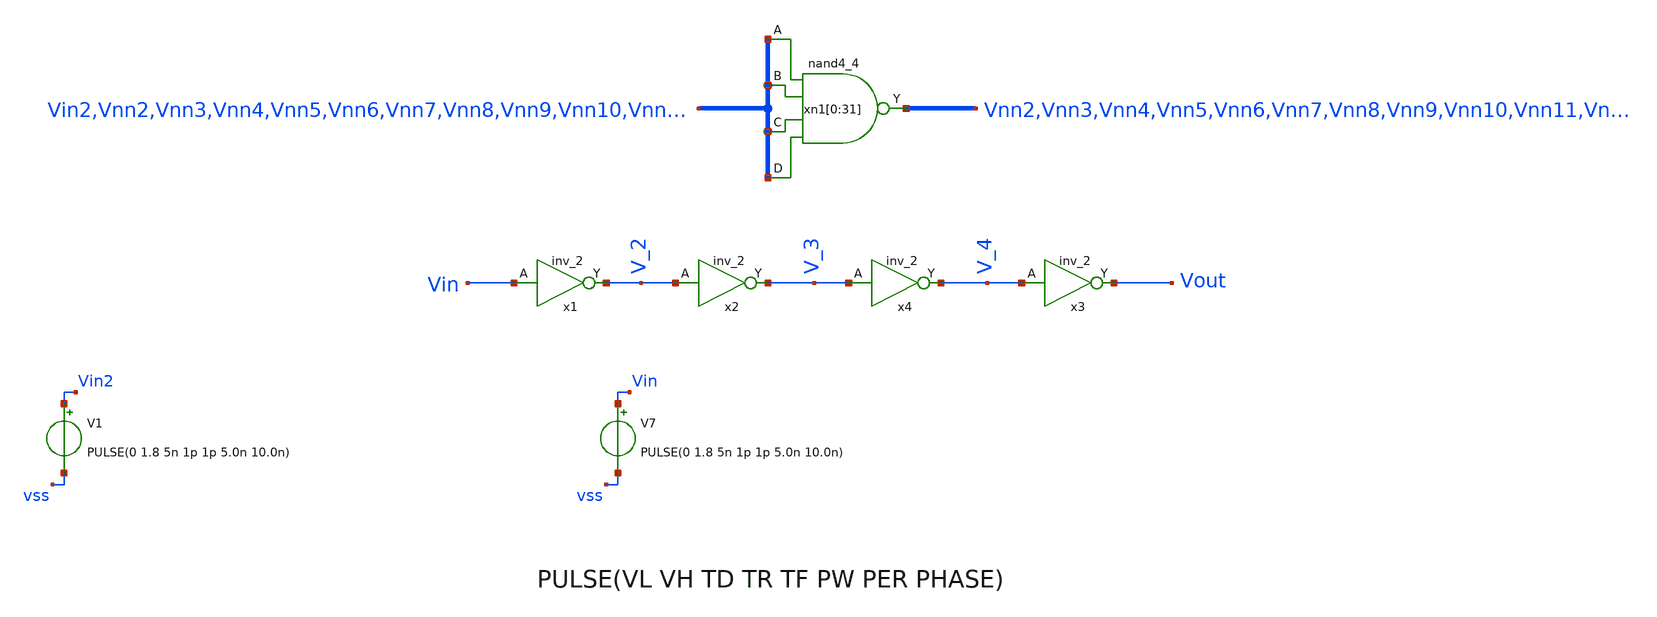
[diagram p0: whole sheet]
** sch_path: TDC_test.sch
.lib $::SKYWATER_MODELS/sky130.lib.spice tt
.include $::SKYWATER_STDCELLS/sky130_fd_sc_hd.spice

**.subckt TDC_test
x1 Vin VSS VSS VCC VCC V_2 sky130_fd_sc_hd__inv_2
x2 V_2 VSS VSS VCC VCC V_3 sky130_fd_sc_hd__inv_2
x3 V_4 VSS VSS VCC VCC Vout sky130_fd_sc_hd__inv_2
V7 Vin vss PULSE(0 1.8 5n 1p 1p 5.0n 10.0n)
x4 V_3 VSS VSS VCC VCC V_4 sky130_fd_sc_hd__inv_2
V1 Vin2 vss PULSE(0 1.8 5n 1p 1p 5.0n 10.0n)
xn1[0] Vin2 Vin2 Vin2 Vin2 VSS VSS VCC VCC Vnn2 sky130_fd_sc_hd__nand4_4
xn1[1] Vnn2 Vnn2 Vnn2 Vnn2 VSS VSS VCC VCC Vnn3 sky130_fd_sc_hd__nand4_4
xn1[2] Vnn3 Vnn3 Vnn3 Vnn3 VSS VSS VCC VCC Vnn4 sky130_fd_sc_hd__nand4_4
xn1[3] Vnn4 Vnn4 Vnn4 Vnn4 VSS VSS VCC VCC Vnn5 sky130_fd_sc_hd__nand4_4
xn1[4] Vnn5 Vnn5 Vnn5 Vnn5 VSS VSS VCC VCC Vnn6 sky130_fd_sc_hd__nand4_4
xn1[5] Vnn6 Vnn6 Vnn6 Vnn6 VSS VSS VCC VCC Vnn7 sky130_fd_sc_hd__nand4_4
xn1[6] Vnn7 Vnn7 Vnn7 Vnn7 VSS VSS VCC VCC Vnn8 sky130_fd_sc_hd__nand4_4
xn1[7] Vnn8 Vnn8 Vnn8 Vnn8 VSS VSS VCC VCC Vnn9 sky130_fd_sc_hd__nand4_4
xn1[8] Vnn9 Vnn9 Vnn9 Vnn9 VSS VSS VCC VCC Vnn10 sky130_fd_sc_hd__nand4_4
xn1[9] Vnn10 Vnn10 Vnn10 Vnn10 VSS VSS VCC VCC Vnn11 sky130_fd_sc_hd__nand4_4
xn1[10] Vnn11 Vnn11 Vnn11 Vnn11 VSS VSS VCC VCC Vnn12 sky130_fd_sc_hd__nand4_4
xn1[11] Vnn12 Vnn12 Vnn12 Vnn12 VSS VSS VCC VCC Vnn13 sky130_fd_sc_hd__nand4_4
xn1[12] Vnn13 Vnn13 Vnn13 Vnn13 VSS VSS VCC VCC Vnn14 sky130_fd_sc_hd__nand4_4
xn1[13] Vnn14 Vnn14 Vnn14 Vnn14 VSS VSS VCC VCC Vnn15 sky130_fd_sc_hd__nand4_4
xn1[14] Vnn15 Vnn15 Vnn15 Vnn15 VSS VSS VCC VCC Vnn16 sky130_fd_sc_hd__nand4_4
xn1[15] Vnn16 Vnn16 Vnn16 Vnn16 VSS VSS VCC VCC Vnn17 sky130_fd_sc_hd__nand4_4
xn1[16] Vnn17 Vnn17 Vnn17 Vnn17 VSS VSS VCC VCC Vnn18 sky130_fd_sc_hd__nand4_4
xn1[17] Vnn18 Vnn18 Vnn18 Vnn18 VSS VSS VCC VCC Vnn19 sky130_fd_sc_hd__nand4_4
xn1[18] Vnn19 Vnn19 Vnn19 Vnn19 VSS VSS VCC VCC Vnn20 sky130_fd_sc_hd__nand4_4
xn1[19] Vnn20 Vnn20 Vnn20 Vnn20 VSS VSS VCC VCC Vnn21 sky130_fd_sc_hd__nand4_4
xn1[20] Vnn21 Vnn21 Vnn21 Vnn21 VSS VSS VCC VCC Vnn22 sky130_fd_sc_hd__nand4_4
xn1[21] Vnn22 Vnn22 Vnn22 Vnn22 VSS VSS VCC VCC Vnn23 sky130_fd_sc_hd__nand4_4
xn1[22] Vnn23 Vnn23 Vnn23 Vnn23 VSS VSS VCC VCC Vnn24 sky130_fd_sc_hd__nand4_4
xn1[23] Vnn24 Vnn24 Vnn24 Vnn24 VSS VSS VCC VCC Vnn25 sky130_fd_sc_hd__nand4_4
xn1[24] Vnn25 Vnn25 Vnn25 Vnn25 VSS VSS VCC VCC Vnn26 sky130_fd_sc_hd__nand4_4
xn1[25] Vnn26 Vnn26 Vnn26 Vnn26 VSS VSS VCC VCC Vnn27 sky130_fd_sc_hd__nand4_4
xn1[26] Vnn27 Vnn27 Vnn27 Vnn27 VSS VSS VCC VCC Vnn28 sky130_fd_sc_hd__nand4_4
xn1[27] Vnn28 Vnn28 Vnn28 Vnn28 VSS VSS VCC VCC Vnn29 sky130_fd_sc_hd__nand4_4
xn1[28] Vnn29 Vnn29 Vnn29 Vnn29 VSS VSS VCC VCC Vnn30 sky130_fd_sc_hd__nand4_4
xn1[29] Vnn30 Vnn30 Vnn30 Vnn30 VSS VSS VCC VCC Vnn31 sky130_fd_sc_hd__nand4_4
xn1[30] Vnn31 Vnn31 Vnn31 Vnn31 VSS VSS VCC VCC Vnn32 sky130_fd_sc_hd__nand4_4
xn1[31] Vnn32 Vnn32 Vnn32 Vnn32 VSS VSS VCC VCC Vout2 sky130_fd_sc_hd__nand4_4
**** begin user architecture code

vvcc vcc 0 dc 1.8
vvss vss 0 0
*.option temp = 0
.save v(Vin) v(Vout) v(Vin2) v(Vout2)
.measure tran tprop TRIG v(Vin) TD=0n VAL=0.9 RISE=1 TARG v(Vout) TD=0n VAL=0.9 RISE=1
.measure tran tprop2 TRIG v(Vin2) TD=0n VAL=0.9 RISE=1 TARG v(Vout2) TD=0n VAL=0.9 RISE=1

.control
   tran 50p 12n
   run
   write TT_3stage_RO_v1p1.raw
*   wrdata /foss/designs/TT_temptodig_ROstudy/TT_3stage_RO_v1p1.txt v(Vnn1)
   plot v(Vin) v(Vout)
   plot v(Vin2) v(Vout2)

.endc


**** end user architecture code
**.ends
.end
